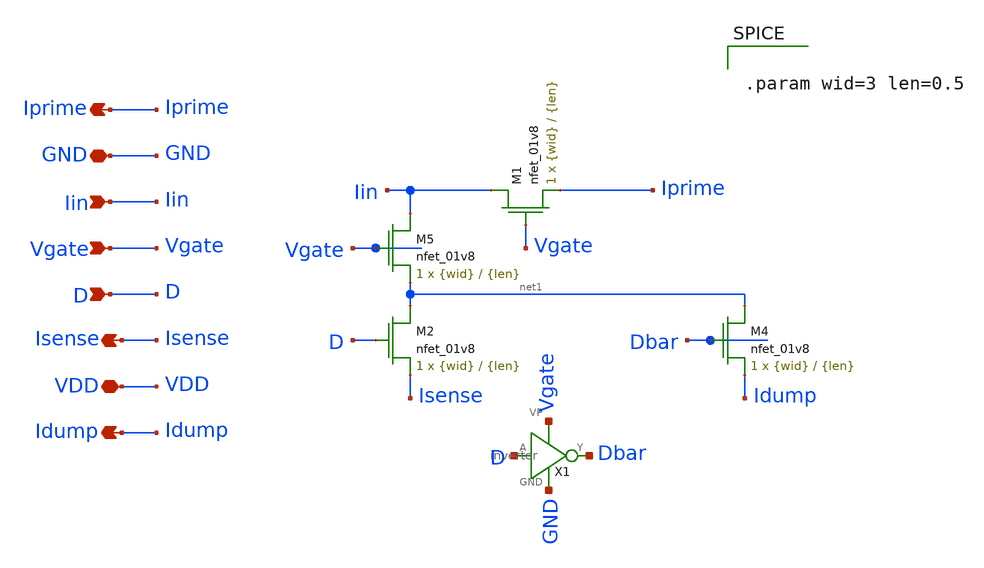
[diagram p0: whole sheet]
** sch_path: final/LDS/daccell_LDS.sch
**.subckt daccell_LDS GND VDD Isense Idump Iin Iprime Vgate D
*.iopin GND
*.iopin VDD
*.opin Isense
*.opin Idump
*.ipin Iin
*.opin Iprime
*.ipin Vgate
*.ipin D
XM5 Iin Vgate net1 GND sky130_fd_pr__nfet_01v8 L={len} W={wid} nf=1 ad='int((nf+1)/2) * W/nf * 0.29'
+ as='int((nf+2)/2) * W/nf * 0.29' pd='2*int((nf+1)/2) * (W/nf + 0.29)' ps='2*int((nf+2)/2) * (W/nf + 0.29)'
+ nrd='0.29 / W' nrs='0.29 / W' sa=0 sb=0 sd=0 mult=1 m=1
XM2 net1 D Isense GND sky130_fd_pr__nfet_01v8 L={len} W={wid} nf=1 ad='int((nf+1)/2) * W/nf * 0.29' as='int((nf+2)/2) * W/nf * 0.29'
+ pd='2*int((nf+1)/2) * (W/nf + 0.29)' ps='2*int((nf+2)/2) * (W/nf + 0.29)' nrd='0.29 / W' nrs='0.29 / W'
+ sa=0 sb=0 sd=0 mult=1 m=1
XM4 net1 Dbar Idump GND sky130_fd_pr__nfet_01v8 L={len} W={wid} nf=1 ad='int((nf+1)/2) * W/nf * 0.29'
+ as='int((nf+2)/2) * W/nf * 0.29' pd='2*int((nf+1)/2) * (W/nf + 0.29)' ps='2*int((nf+2)/2) * (W/nf + 0.29)'
+ nrd='0.29 / W' nrs='0.29 / W' sa=0 sb=0 sd=0 mult=1 m=1
XM1 Iin Vgate Iprime GND sky130_fd_pr__nfet_01v8 L={len} W={wid} nf=1 ad='int((nf+1)/2) * W/nf * 0.29'
+ as='int((nf+2)/2) * W/nf * 0.29' pd='2*int((nf+1)/2) * (W/nf + 0.29)' ps='2*int((nf+2)/2) * (W/nf + 0.29)'
+ nrd='0.29 / W' nrs='0.29 / W' sa=0 sb=0 sd=0 mult=1 m=1
X1 Vgate D Dbar GND inverter
**** begin user architecture code


.param wid=3 len=0.5


**** end user architecture code
**.ends

* expanding   symbol:  inverter.sym # of pins=4
** sym_path: final/LDS/inverter.sym
** sch_path: final/LDS/inverter.sch
.subckt inverter VP A Y GND
*.ipin A
*.iopin VP
*.iopin GND
*.opin Y
**** begin user architecture code


.param wid=3 len=0.5


**** end user architecture code
XM1 Y A VP VDD sky130_fd_pr__pfet_01v8 L={len} W={wid} nf=1 ad='int((nf+1)/2) * W/nf * 0.29' as='int((nf+2)/2) * W/nf * 0.29'
+ pd='2*int((nf+1)/2) * (W/nf + 0.29)' ps='2*int((nf+2)/2) * (W/nf + 0.29)' nrd='0.29 / W' nrs='0.29 / W'
+ sa=0 sb=0 sd=0 mult=1 m=1
XM2 Y A GND GND sky130_fd_pr__nfet_01v8 L={len} W={wid} nf=1 ad='int((nf+1)/2) * W/nf * 0.29' as='int((nf+2)/2) * W/nf * 0.29'
+ pd='2*int((nf+1)/2) * (W/nf + 0.29)' ps='2*int((nf+2)/2) * (W/nf + 0.29)' nrd='0.29 / W' nrs='0.29 / W'
+ sa=0 sb=0 sd=0 mult=1 m=1
.ends

.end
